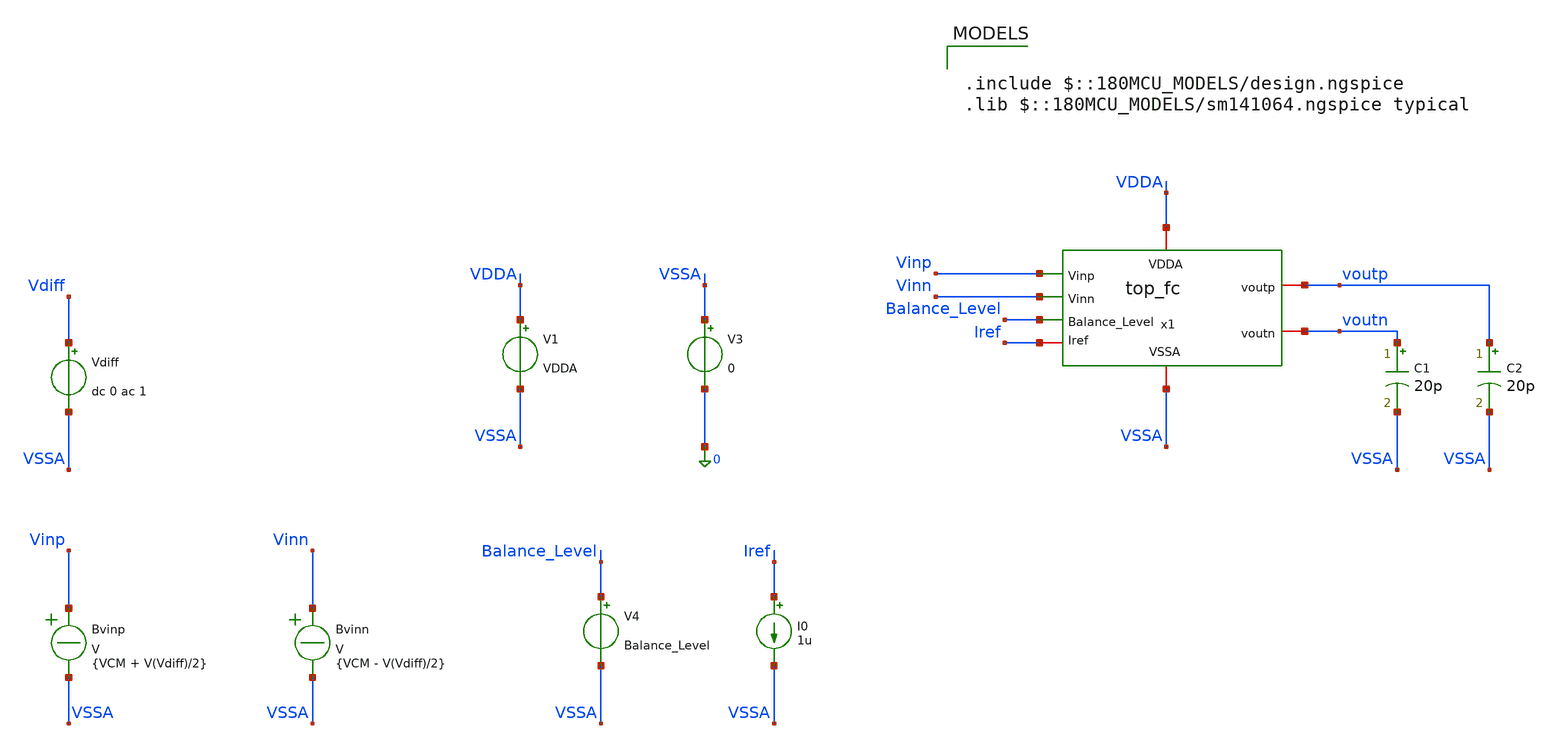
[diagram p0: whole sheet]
** sch_path: Folded_cascode/testbenches/top_fc_noise_tb.sch
**.subckt top_fc_noise_tb
x1 Balance_Level Vinp voutp VDDA voutn Vinn Iref VSSA top_fc
C1 voutn VSSA 20p m=1
C2 voutp VSSA 20p m=1
V1 VDDA VSSA VDDA
V3 VSSA 0 0
V4 Balance_Level VSSA Balance_Level
I0 Iref VSSA 1u
Bvinp Vinp VSSA V = {VCM + V(Vdiff)/2}
Bvinn Vinn VSSA V = {VCM - V(Vdiff)/2}
Vdiff Vdiff VSSA dc 0 ac 1
**** begin user architecture code

.include $::180MCU_MODELS/design.ngspice
.lib $::180MCU_MODELS/sm141064.ngspice typical



.temp 27
.param VDDA = 5
.param Balance_Level = 1.5
.param VCM = 2.5
.param sw_stat_global=0
.param sw_stat_mismatch=0

.control
option sparse
set filetype=ascii
set wr_singlescale
set wr_vecnames
save all
save @m.x1.x1.xm1.m0[id]
save @m.x1.x1.xm1.m0[gm]
save @m.x1.x1.xm1.m0[vgs]
save @m.x1.x1.xm1.m0[vds]
save @m.x1.x1.xm1.m0[vth]
save @m.x1.x1.xm1.m0[gds]
save @m.x1.x1.xm1.m0[vdsat]

save @m.x1.x1.xm2.m0[id]
save @m.x1.x1.xm2.m0[gm]
save @m.x1.x1.xm2.m0[vgs]
save @m.x1.x1.xm2.m0[vds]
save @m.x1.x1.xm2.m0[vth]
save @m.x1.x1.xm2.m0[gds]
save @m.x1.x1.xm2.m0[vdsat]

save @m.x1.x1.xm9.m0[id]
save @m.x1.x1.xm9.m0[gm]
save @m.x1.x1.xm9.m0[vgs]
save @m.x1.x1.xm9.m0[vds]
save @m.x1.x1.xm9.m0[vth]
save @m.x1.x1.xm9.m0[gds]
save @m.x1.x1.xm9.m0[vdsat]

save @m.x1.x1.xm8.m0[id]
save @m.x1.x1.xm8.m0[gm]
save @m.x1.x1.xm8.m0[vgs]
save @m.x1.x1.xm8.m0[vds]
save @m.x1.x1.xm8.m0[vth]
save @m.x1.x1.xm8.m0[gds]
save @m.x1.x1.xm8.m0[vdsat]

save @m.x1.x1.xm6.m0[id]
save @m.x1.x1.xm6.m0[gm]
save @m.x1.x1.xm6.m0[vgs]
save @m.x1.x1.xm6.m0[vds]
save @m.x1.x1.xm6.m0[vth]
save @m.x1.x1.xm6.m0[gds]
save @m.x1.x1.xm6.m0[vdsat]

save @m.x1.x1.xm5.m0[id]
save @m.x1.x1.xm5.m0[gm]
save @m.x1.x1.xm5.m0[vgs]
save @m.x1.x1.xm5.m0[vds]
save @m.x1.x1.xm5.m0[vth]
save @m.x1.x1.xm5.m0[gds]
save @m.x1.x1.xm5.m0[vdsat]

save @m.x1.x2.xm1.m0[id]
save @m.x1.x2.xm1.m0[gm]
save @m.x1.x2.xm1.m0[vgs]
save @m.x1.x2.xm1.m0[vds]
save @m.x1.x2.xm1.m0[vth]
save @m.x1.x2.xm1.m0[gds]

save @m.x1.x2.xm2.m0[id]
save @m.x1.x2.xm2.m0[gm]
save @m.x1.x2.xm2.m0[vgs]
save @m.x1.x2.xm2.m0[vds]
save @m.x1.x2.xm2.m0[vth]
save @m.x1.x2.xm2.m0[gds]

save @m.x1.x2.xm3.m0[id]
save @m.x1.x2.xm3.m0[gm]
save @m.x1.x2.xm3.m0[vgs]
save @m.x1.x2.xm3.m0[vds]
save @m.x1.x2.xm3.m0[vth]
save @m.x1.x2.xm3.m0[gds]

save @m.x1.x2.xm4.m0[id]
save @m.x1.x2.xm4.m0[gm]
save @m.x1.x2.xm4.m0[vgs]
save @m.x1.x2.xm4.m0[vds]
save @m.x1.x2.xm4.m0[vth]
save @m.x1.x2.xm4.m0[gds]

save @m.x1.x2.xm5.m0[id]
save @m.x1.x2.xm5.m0[gm]
save @m.x1.x2.xm5.m0[vgs]
save @m.x1.x2.xm5.m0[vds]
save @m.x1.x2.xm5.m0[vth]
save @m.x1.x2.xm5.m0[gds]

save @m.x1.x2.xm6.m0[id]
save @m.x1.x2.xm6.m0[gm]
save @m.x1.x2.xm6.m0[vgs]
save @m.x1.x2.xm6.m0[vds]
save @m.x1.x2.xm6.m0[vth]
save @m.x1.x2.xm6.m0[gds]

save @m.x1.x2.xm7.m0[id]
save @m.x1.x2.xm7.m0[gm]
save @m.x1.x2.xm7.m0[vgs]
save @m.x1.x2.xm7.m0[vds]
save @m.x1.x2.xm7.m0[vth]
save @m.x1.x2.xm7.m0[gds]

save @m.x1.x2.xm8.m0[id]
save @m.x1.x2.xm8.m0[gm]
save @m.x1.x2.xm8.m0[vgs]
save @m.x1.x2.xm8.m0[vds]
save @m.x1.x2.xm8.m0[vth]
save @m.x1.x2.xm8.m0[gds]

save @m.x1.x2.xm9.m0[id]
save @m.x1.x2.xm9.m0[gm]
save @m.x1.x2.xm9.m0[vgs]
save @m.x1.x2.xm9.m0[vds]
save @m.x1.x2.xm9.m0[vth]
save @m.x1.x2.xm9.m0[gds]

save @m.x1.x3.xm1.m0[id]
save @m.x1.x3.xm1.m0[gm]
save @m.x1.x3.xm1.m0[vgs]
save @m.x1.x3.xm1.m0[vds]
save @m.x1.x3.xm1.m0[vth]
save @m.x1.x3.xm1.m0[gds]

save @m.x1.x3.xm2.m0[id]
save @m.x1.x3.xm2.m0[gm]
save @m.x1.x3.xm2.m0[vgs]
save @m.x1.x3.xm2.m0[vds]
save @m.x1.x3.xm2.m0[vth]
save @m.x1.x3.xm2.m0[gds]

save @m.x1.x3.xm3.m0[id]
save @m.x1.x3.xm3.m0[gm]
save @m.x1.x3.xm3.m0[vgs]
save @m.x1.x3.xm3.m0[vds]
save @m.x1.x3.xm3.m0[vth]
save @m.x1.x3.xm3.m0[gds]

save @m.x1.x3.xm4.m0[id]
save @m.x1.x3.xm4.m0[gm]
save @m.x1.x3.xm4.m0[vgs]
save @m.x1.x3.xm4.m0[vds]
save @m.x1.x3.xm4.m0[vth]
save @m.x1.x3.xm4.m0[gds]

save @m.x1.x3.xm5.m0[id]
save @m.x1.x3.xm5.m0[gm]
save @m.x1.x3.xm5.m0[vgs]
save @m.x1.x3.xm5.m0[vds]
save @m.x1.x3.xm5.m0[vth]
save @m.x1.x3.xm5.m0[gds]

save @m.x1.x3.xm6.m0[id]
save @m.x1.x3.xm6.m0[gm]
save @m.x1.x3.xm6.m0[vgs]
save @m.x1.x3.xm6.m0[vds]
save @m.x1.x3.xm6.m0[vth]
save @m.x1.x3.xm6.m0[gds]

save @m.x1.x3.xm7.m0[id]
save @m.x1.x3.xm7.m0[gm]
save @m.x1.x3.xm7.m0[vgs]
save @m.x1.x3.xm7.m0[vds]
save @m.x1.x3.xm7.m0[vth]
save @m.x1.x3.xm7.m0[gds]

save @m.x1.x3.xm8.m0[id]
save @m.x1.x3.xm8.m0[gm]
save @m.x1.x3.xm8.m0[vgs]
save @m.x1.x3.xm8.m0[vds]
save @m.x1.x3.xm8.m0[vth]
save @m.x1.x3.xm8.m0[gds]

save @m.x1.x3.xm9.m0[id]
save @m.x1.x3.xm9.m0[gm]
save @m.x1.x3.xm9.m0[vgs]
save @m.x1.x3.xm9.m0[vds]
save @m.x1.x3.xm9.m0[vth]
save @m.x1.x3.xm9.m0[gds]

save @m.x1.x3.xm10.m0[id]
save @m.x1.x3.xm10.m0[gm]
save @m.x1.x3.xm10.m0[vgs]
save @m.x1.x3.xm10.m0[vds]
save @m.x1.x3.xm10.m0[vth]
save @m.x1.x3.xm10.m0[gds]

save @m.x1.x3.xm11.m0[id]
save @m.x1.x3.xm11.m0[gm]
save @m.x1.x3.xm11.m0[vgs]
save @m.x1.x3.xm11.m0[vds]
save @m.x1.x3.xm11.m0[vth]
save @m.x1.x3.xm11.m0[gds]

save @m.x1.x3.xm12.m0[id]
save @m.x1.x3.xm12.m0[gm]
save @m.x1.x3.xm12.m0[vgs]
save @m.x1.x3.xm12.m0[vds]
save @m.x1.x3.xm12.m0[vth]
save @m.x1.x3.xm12.m0[gds]

save @m.x1.x3.xm13.m0[id]
save @m.x1.x3.xm13.m0[gm]
save @m.x1.x3.xm13.m0[vgs]
save @m.x1.x3.xm13.m0[vds]
save @m.x1.x3.xm13.m0[vth]
save @m.x1.x3.xm13.m0[gds]

save @m.x1.x3.xm14.m0[id]
save @m.x1.x3.xm14.m0[gm]
save @m.x1.x3.xm14.m0[vgs]
save @m.x1.x3.xm14.m0[vds]
save @m.x1.x3.xm14.m0[vth]
save @m.x1.x3.xm14.m0[gds]

save @m.x1.x3.xm15.m0[id]
save @m.x1.x3.xm15.m0[gm]
save @m.x1.x3.xm15.m0[vgs]
save @m.x1.x3.xm15.m0[vds]
save @m.x1.x3.xm15.m0[vth]
save @m.x1.x3.xm15.m0[gds]

save @m.x1.x3.xm16.m0[id]
save @m.x1.x3.xm16.m0[gm]
save @m.x1.x3.xm16.m0[vgs]
save @m.x1.x3.xm16.m0[vds]
save @m.x1.x3.xm16.m0[vth]
save @m.x1.x3.xm16.m0[gds]

save @m.x1.x3.xm17.m0[id]
save @m.x1.x3.xm17.m0[gm]
save @m.x1.x3.xm17.m0[vgs]
save @m.x1.x3.xm17.m0[vds]
save @m.x1.x3.xm17.m0[vth]
save @m.x1.x3.xm17.m0[gds]

save @m.x1.x3.xm18.m0[id]
save @m.x1.x3.xm18.m0[gm]
save @m.x1.x3.xm18.m0[vgs]
save @m.x1.x3.xm18.m0[vds]
save @m.x1.x3.xm18.m0[vth]
save @m.x1.x3.xm18.m0[gds]

save @m.x1.x3.xm21.m0[id]
save @m.x1.x3.xm21.m0[gm]
save @m.x1.x3.xm21.m0[vgs]
save @m.x1.x3.xm21.m0[vds]
save @m.x1.x3.xm21.m0[vth]
save @m.x1.x3.xm21.m0[gds]

save @m.x1.x3.xm22.m0[id]
save @m.x1.x3.xm22.m0[gm]
save @m.x1.x3.xm22.m0[vgs]
save @m.x1.x3.xm22.m0[vds]
save @m.x1.x3.xm22.m0[vth]
save @m.x1.x3.xm22.m0[gds]

op
write top_fc_op_tb.raw all

* ------------------------------------------------------------
* Noise analysis
* ------------------------------------------------------------

noise v(voutp,voutn) Vdiff dec 100 1 100Meg


* ============================================================
* NOISE SPECTRAL DENSITY
*
* noise1 contains:
*
*   frequency
*   onoise_spectrum
*   inoise_spectrum
*
* Units:
*
*   onoise_spectrum : V/sqrt(Hz)
*   inoise_spectrum : V/sqrt(Hz)
* ============================================================

setplot noise1

plot onoise_spectrum
plot inoise_spectrum


* ------------------------------------------------------------
* Export spectrum
*
* Columns:
*   frequency
*   onoise_spectrum
*   inoise_spectrum
* ------------------------------------------------------------

wrdata noise_spectrum.dat onoise_spectrum inoise_spectrum


* ------------------------------------------------------------
* Save spectral raw data
* ------------------------------------------------------------

write top_fc_noise_spectrum_tb.raw


* ============================================================
* INTEGRATED NOISE
*
* noise2 contains the integrated noise over the entire
* simulated frequency range.
* ============================================================

setplot noise2

print onoise_total
print inoise_total

.endc


**** end user architecture code
**.ends
.end
